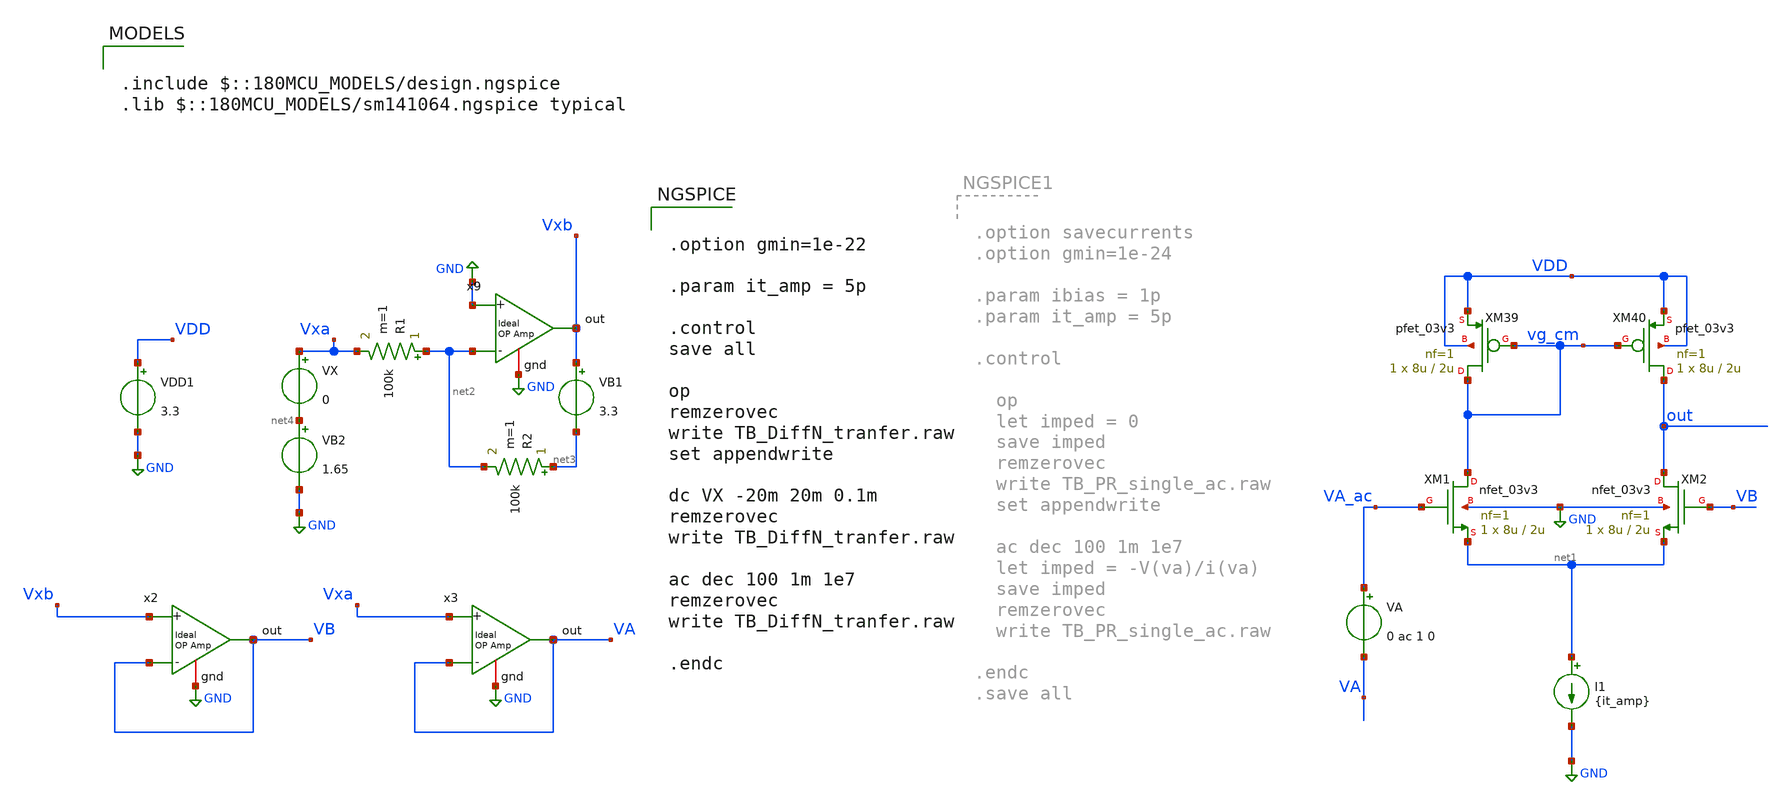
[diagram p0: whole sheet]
** sch_path: TIA/xschem/PseudoResistor/TB_DiffN_tranfer.sch
**.subckt TB_DiffN_tranfer
XM1 vg_cm VA_ac net1 GND nfet_03v3 L=2u W=8u nf=1 ad='int((nf+1)/2) * W/nf * 0.18u' as='int((nf+2)/2) * W/nf * 0.18u'
+ pd='2*int((nf+1)/2) * (W/nf + 0.18u)' ps='2*int((nf+2)/2) * (W/nf + 0.18u)' nrd='0.18u / W' nrs='0.18u / W'
+ sa=0 sb=0 sd=0 m=1
XM2 out VB net1 GND nfet_03v3 L=2u W=8u nf=1 ad='int((nf+1)/2) * W/nf * 0.18u' as='int((nf+2)/2) * W/nf * 0.18u'
+ pd='2*int((nf+1)/2) * (W/nf + 0.18u)' ps='2*int((nf+2)/2) * (W/nf + 0.18u)' nrd='0.18u / W' nrs='0.18u / W'
+ sa=0 sb=0 sd=0 m=1
XM39 vg_cm vg_cm VDD VDD pfet_03v3 L=2u W=8u nf=1 ad='int((nf+1)/2) * W/nf * 0.18u' as='int((nf+2)/2) * W/nf * 0.18u'
+ pd='2*int((nf+1)/2) * (W/nf + 0.18u)' ps='2*int((nf+2)/2) * (W/nf + 0.18u)' nrd='0.18u / W' nrs='0.18u / W'
+ sa=0 sb=0 sd=0 m=1
XM40 out vg_cm VDD VDD pfet_03v3 L=2u W=8u nf=1 ad='int((nf+1)/2) * W/nf * 0.18u' as='int((nf+2)/2) * W/nf * 0.18u'
+ pd='2*int((nf+1)/2) * (W/nf + 0.18u)' ps='2*int((nf+2)/2) * (W/nf + 0.18u)' nrd='0.18u / W' nrs='0.18u / W'
+ sa=0 sb=0 sd=0 m=1
I1 net1 GND {it_amp}
VDD1 VDD GND 3.3
VX Vxa net4 0
VB1 Vxb net3 3.3
R1 net2 Vxa 100k m=1
R2 net3 net2 100k m=1
VB2 net4 GND 1.65
x2 VB Vxb VB GND ampOp_ideal
x3 VA Vxa VA GND ampOp_ideal
x9 Vxb GND net2 GND ampOp_ideal
VA VA_ac VA 0 ac 1 0
**** begin user architecture code


.option gmin=1e-22

.param it_amp = 5p

.control
save all

op
remzerovec
write TB_DiffN_tranfer.raw
set appendwrite

dc VX -20m 20m 0.1m
remzerovec
write TB_DiffN_tranfer.raw

ac dec 100 1m 1e7
remzerovec
write TB_DiffN_tranfer.raw

.endc



.include $::180MCU_MODELS/design.ngspice
.lib $::180MCU_MODELS/sm141064.ngspice typical

**** end user architecture code
**.ends

* expanding   symbol:  /home/gmaranhao/Desktop/gf180_work/auxLib/ampOp_ideal.sym # of pins=4
** sym_path: /home/gmaranhao/Desktop/gf180_work/auxLib/ampOp_ideal.sym
** sch_path: /home/gmaranhao/Desktop/gf180_work/auxLib/ampOp_ideal.sch
.subckt ampOp_ideal out + - gnd
*.ipin +
*.ipin -
*.opin out
*.iopin gnd
E1 out gnd + - 10000000
.ends

.GLOBAL GND
.end
